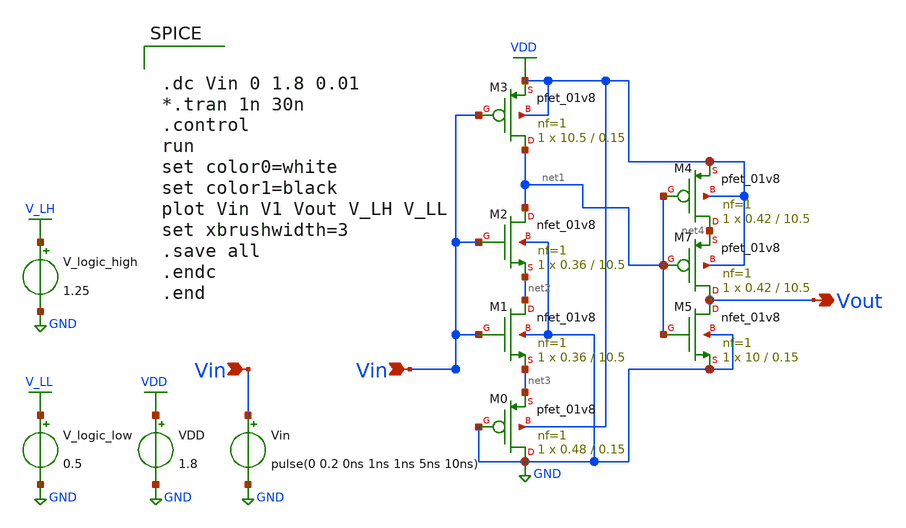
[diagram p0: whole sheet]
** sch_path: xschem/Vth_sch/th15.sch
**.subckt th15 Vin Vin Vout
*.ipin Vin
*.ipin Vin
*.opin Vout
VDD VDD GND 1.8
Vin Vin GND pulse(0 0.2 0ns 1ns 1ns 5ns 10ns)
V_logic_high V_LH GND 1.25
V_logic_low V_LL GND 0.5
XM0 GND GND net3 VDD sky130_fd_pr__pfet_01v8 L=0.15 W=0.48 nf=1 ad='int((nf+1)/2) * W/nf * 0.29' as='int((nf+2)/2) * W/nf * 0.29'
+ pd='2*int((nf+1)/2) * (W/nf + 0.29)' ps='2*int((nf+2)/2) * (W/nf + 0.29)' nrd='0.29 / W' nrs='0.29 / W'
+ sa=0 sb=0 sd=0 mult=1 m=1
XM1 net2 Vin net3 GND sky130_fd_pr__nfet_01v8 L=10.5 W=0.36 nf=1 ad='int((nf+1)/2) * W/nf * 0.29' as='int((nf+2)/2) * W/nf * 0.29'
+ pd='2*int((nf+1)/2) * (W/nf + 0.29)' ps='2*int((nf+2)/2) * (W/nf + 0.29)' nrd='0.29 / W' nrs='0.29 / W'
+ sa=0 sb=0 sd=0 mult=1 m=1
XM2 net1 Vin net2 GND sky130_fd_pr__nfet_01v8 L=10.5 W=0.36 nf=1 ad='int((nf+1)/2) * W/nf * 0.29' as='int((nf+2)/2) * W/nf * 0.29'
+ pd='2*int((nf+1)/2) * (W/nf + 0.29)' ps='2*int((nf+2)/2) * (W/nf + 0.29)' nrd='0.29 / W' nrs='0.29 / W'
+ sa=0 sb=0 sd=0 mult=1 m=1
XM3 net1 Vin VDD VDD sky130_fd_pr__pfet_01v8 L=0.15 W=10.5 nf=1 ad='int((nf+1)/2) * W/nf * 0.29' as='int((nf+2)/2) * W/nf * 0.29'
+ pd='2*int((nf+1)/2) * (W/nf + 0.29)' ps='2*int((nf+2)/2) * (W/nf + 0.29)' nrd='0.29 / W' nrs='0.29 / W'
+ sa=0 sb=0 sd=0 mult=1 m=1
XM4 net4 net1 VDD VDD sky130_fd_pr__pfet_01v8 L=10.5 W=0.42 nf=1 ad='int((nf+1)/2) * W/nf * 0.29' as='int((nf+2)/2) * W/nf * 0.29'
+ pd='2*int((nf+1)/2) * (W/nf + 0.29)' ps='2*int((nf+2)/2) * (W/nf + 0.29)' nrd='0.29 / W' nrs='0.29 / W'
+ sa=0 sb=0 sd=0 mult=1 m=1
XM7 Vout net1 net4 VDD sky130_fd_pr__pfet_01v8 L=10.5 W=0.42 nf=1 ad='int((nf+1)/2) * W/nf * 0.29' as='int((nf+2)/2) * W/nf * 0.29'
+ pd='2*int((nf+1)/2) * (W/nf + 0.29)' ps='2*int((nf+2)/2) * (W/nf + 0.29)' nrd='0.29 / W' nrs='0.29 / W'
+ sa=0 sb=0 sd=0 mult=1 m=1
XM5 Vout net1 GND GND sky130_fd_pr__nfet_01v8 L=0.15 W=10 nf=1 ad='int((nf+1)/2) * W/nf * 0.29' as='int((nf+2)/2) * W/nf * 0.29'
+ pd='2*int((nf+1)/2) * (W/nf + 0.29)' ps='2*int((nf+2)/2) * (W/nf + 0.29)' nrd='0.29 / W' nrs='0.29 / W'
+ sa=0 sb=0 sd=0 mult=1 m=1
**** begin user architecture code


.lib /usr/local/share/pdk/sky130A/libs.tech/ngspice/sky130.lib.spice tt

.save all





.dc Vin 0 1.8 0.01
*.tran 1n 30n
.control
run
set color0=white
set color1=black
plot Vin V1 Vout V_LH V_LL
set xbrushwidth=3
.save all
.endc
.end


**** end user architecture code
**.ends
.GLOBAL VDD
.GLOBAL GND
.GLOBAL V_LH
.GLOBAL V_LL
.end
